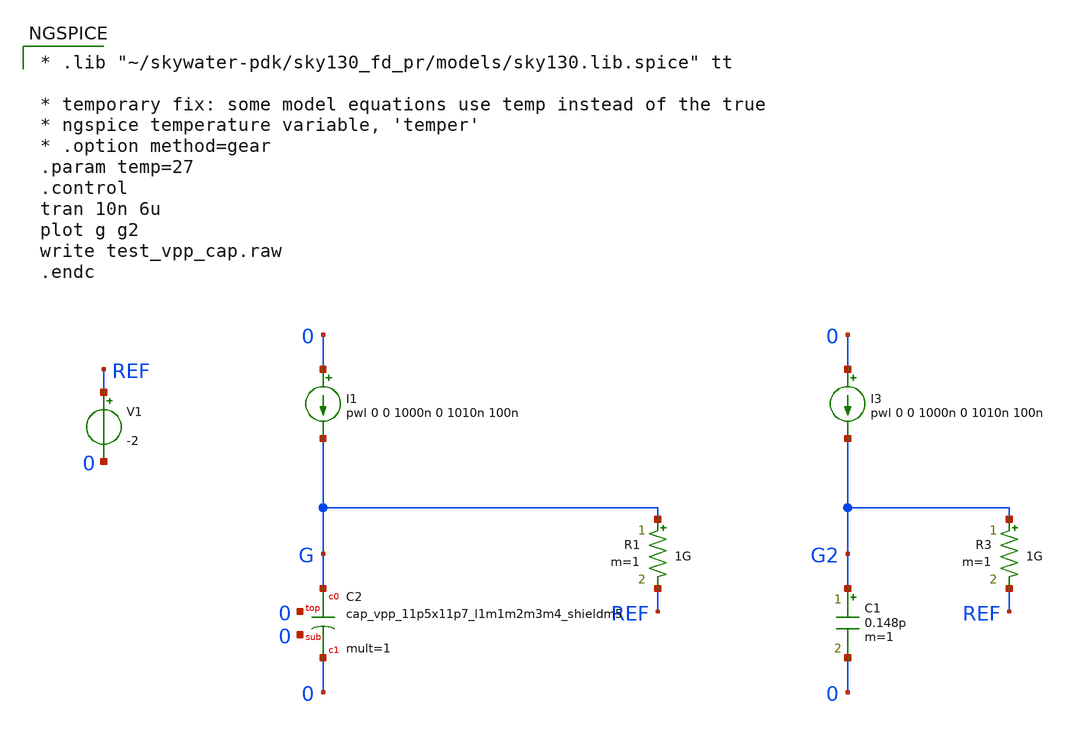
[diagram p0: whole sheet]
** sch_path: sky130_tests/test_vpp_cap.sch
* Copyright 2020 Stefan Frederik Schippers
* Licensed under the Apache License, Version 2.0 (the "License");
* you may not use this file except in compliance with the License.
* You may obtain a copy of the License at
* https://www.apache.org/licenses/LICENSE-2.0
* Unless required by applicable law or agreed to in writing, software
* distributed under the License is distributed on an "AS IS" BASIS,
* WITHOUT WARRANTIES OR CONDITIONS OF ANY KIND, either express or implied.
* See the License for the specific language governing permissions and
* limitations under the License.
**.subckt test_vpp_cap
I1 0 G pwl 0 0 1000n 0 1010n 100n
R1 G REF 1G m=1
I3 0 G2 pwl 0 0 1000n 0 1010n 100n
R3 G2 REF 1G m=1
C1 G2 0 0.148p m=1
V1 REF 0 -2
XC2 G 0 0 0 sky130_fd_pr__cap_vpp_11p5x11p7_l1m1m2m3m4_shieldm5 W=1 L=1 mult=1
**** begin user architecture code

* .lib "~/skywater-pdk/sky130_fd_pr/models/sky130.lib.spice" tt

* temporary fix: some model equations use temp instead of the true
* ngspice temperature variable, 'temper'
* .option method=gear
.param temp=27
.control
tran 10n 6u
plot g g2
write test_vpp_cap.raw
.endc


**** end user architecture code
**.ends
**** begin user architecture code

.include   ~/skywater-pdk/sky130_fd_pr_ngspice/cells/nfet_01v8/sky130_fd_pr__nfet_01v8__tt.corner.spice
.include ~/skywater-pdk/sky130_fd_pr_ngspice/cells/nfet_01v8_lvt/sky130_fd_pr__nfet_01v8_lvt__tt.corner.spice
.include ~/skywater-pdk/sky130_fd_pr_ngspice/cells/pfet_01v8/sky130_fd_pr__pfet_01v8__tt.corner.spice
.include ~/skywater-pdk/sky130_fd_pr_ngspice/cells/nfet_03v3_nvt/sky130_fd_pr__nfet_03v3_nvt__tt.corner.spice
.include ~/skywater-pdk/sky130_fd_pr_ngspice/cells/nfet_05v0_nvt/sky130_fd_pr__nfet_05v0_nvt__tt.corner.spice
.include ~/skywater-pdk/sky130_fd_pr_ngspice/cells/esd_nfet_01v8/sky130_fd_pr__esd_nfet_01v8__tt.corner.spice
.include ~/skywater-pdk/sky130_fd_pr_ngspice/cells/pfet_01v8_lvt/sky130_fd_pr__pfet_01v8_lvt__tt.corner.spice
.include ~/skywater-pdk/sky130_fd_pr_ngspice/cells/pfet_01v8_hvt/sky130_fd_pr__pfet_01v8_hvt__tt.corner.spice
.include ~/skywater-pdk/sky130_fd_pr_ngspice/cells/esd_pfet_g5v0d10v5/sky130_fd_pr__esd_pfet_g5v0d10v5__tt.corner.spice
.include ~/skywater-pdk/sky130_fd_pr_ngspice/cells/pfet_g5v0d10v5/sky130_fd_pr__pfet_g5v0d10v5__tt.corner.spice
.include ~/skywater-pdk/sky130_fd_pr_ngspice/cells/pfet_g5v0d16v0/sky130_fd_pr__pfet_g5v0d16v0__tt.corner.spice
.include ~/skywater-pdk/sky130_fd_pr_ngspice/cells/nfet_g5v0d10v5/sky130_fd_pr__nfet_g5v0d10v5__tt.corner.spice
.include ~/skywater-pdk/sky130_fd_pr_ngspice/cells/nfet_g5v0d16v0/sky130_fd_pr__nfet_g5v0d16v0__tt_discrete.corner.spice
.include ~/skywater-pdk/sky130_fd_pr_ngspice/cells/esd_nfet_g5v0d10v5/sky130_fd_pr__esd_nfet_g5v0d10v5__tt.corner.spice
.include ~/skywater-pdk/sky130_fd_pr_ngspice/models/corners/tt/nonfet.spice
* Mismatch parameters
.include ~/skywater-pdk/sky130_fd_pr_ngspice/cells/nfet_01v8/sky130_fd_pr__nfet_01v8__mismatch.corner.spice
.include ~/skywater-pdk/sky130_fd_pr_ngspice/cells/pfet_01v8/sky130_fd_pr__pfet_01v8__mismatch.corner.spice
.include ~/skywater-pdk/sky130_fd_pr_ngspice/cells/nfet_01v8_lvt/sky130_fd_pr__nfet_01v8_lvt__mismatch.corner.spice
.include ~/skywater-pdk/sky130_fd_pr_ngspice/cells/pfet_01v8_lvt/sky130_fd_pr__pfet_01v8_lvt__mismatch.corner.spice
.include ~/skywater-pdk/sky130_fd_pr_ngspice/cells/pfet_01v8_hvt/sky130_fd_pr__pfet_01v8_hvt__mismatch.corner.spice
.include ~/skywater-pdk/sky130_fd_pr_ngspice/cells/nfet_g5v0d10v5/sky130_fd_pr__nfet_g5v0d10v5__mismatch.corner.spice
.include ~/skywater-pdk/sky130_fd_pr_ngspice/cells/pfet_g5v0d10v5/sky130_fd_pr__pfet_g5v0d10v5__mismatch.corner.spice
.include ~/skywater-pdk/sky130_fd_pr_ngspice/cells/nfet_05v0_nvt/sky130_fd_pr__nfet_05v0_nvt__mismatch.corner.spice
.include ~/skywater-pdk/sky130_fd_pr_ngspice/cells/nfet_03v3_nvt/sky130_fd_pr__nfet_03v3_nvt__mismatch.corner.spice
* Resistor/Capacitor
.include ~/skywater-pdk/sky130_fd_pr_ngspice/models/r+c/res_typical__cap_typical.spice
.include ~/skywater-pdk/sky130_fd_pr_ngspice/models/r+c/res_typical__cap_typical__lin.spice
* Special cells
.include ~/skywater-pdk/sky130_fd_pr_ngspice/models/corners/tt/specialized_cells.spice
* All models
.include ~/skywater-pdk/sky130_fd_pr_ngspice/models/all.spice
* Corner
.include ~/skywater-pdk/sky130_fd_pr_ngspice/models/corners/tt/rf.spice


**** end user architecture code
.end
